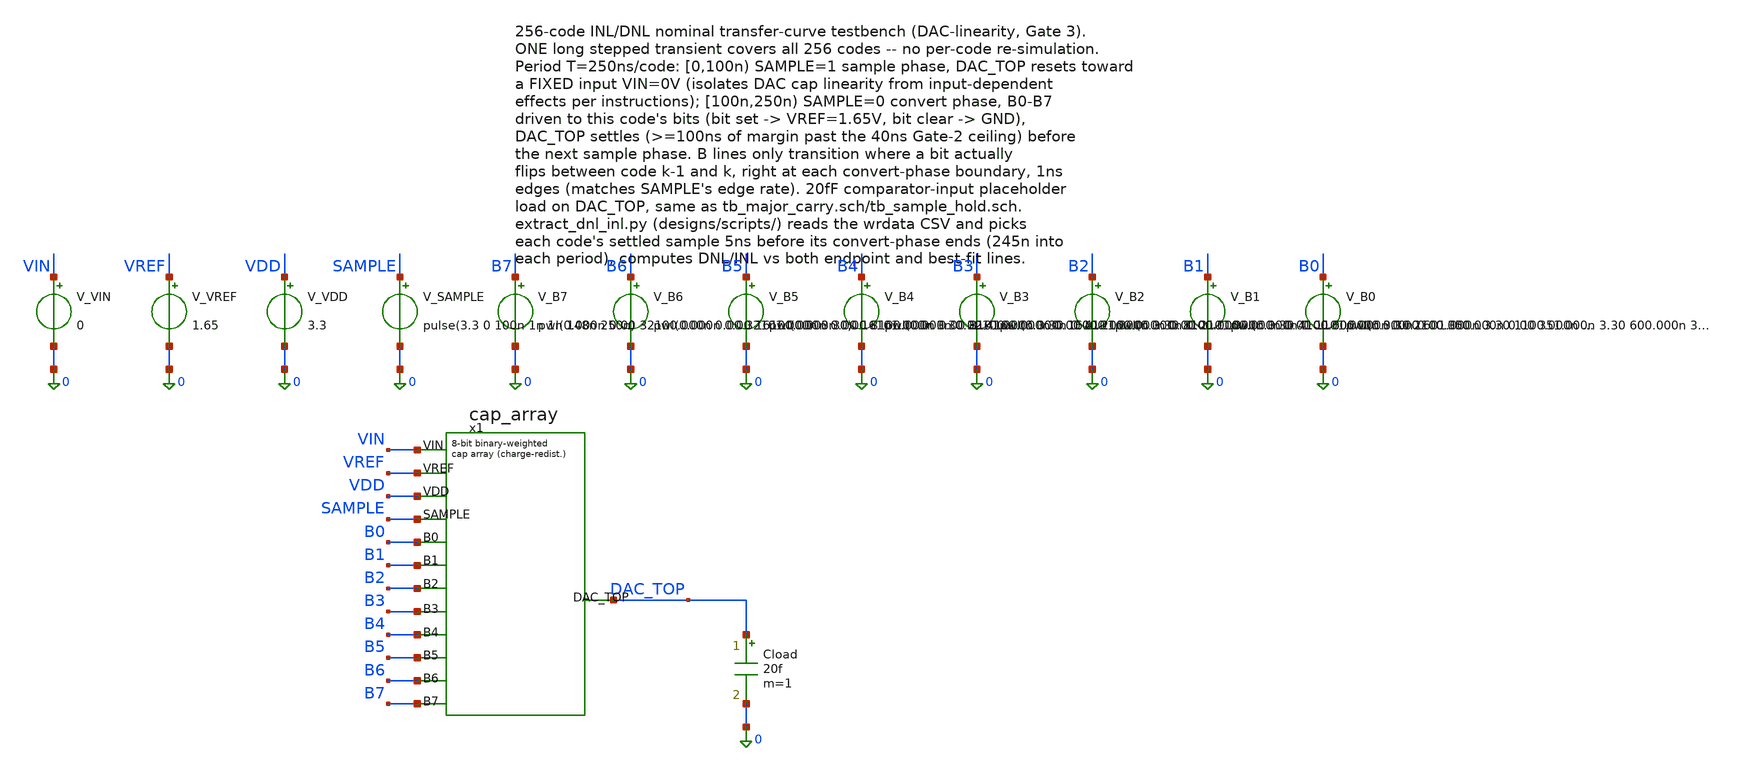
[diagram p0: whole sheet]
** sch_path: dac/sim/tb_inl_dnl.sch
**.subckt tb_inl_dnl
V_VIN VIN 0 0
V_VREF VREF 0 1.65
V_VDD VDD 0 3.3
V_SAMPLE SAMPLE 0 pulse(3.3 0 100n 1n 1n 148n 250n)
V_B7 B7 0 pwl(0.000n 0.00 32100.000n 0.00 32101.000n 3.30)
V_B6 B6 0 pwl(0.000n 0.00 16100.000n 0.00 16101.000n 3.30 32100.000n 3.30 32101.000n 0.00 48100.000n
+ 0.00 48101.000n 3.30)
V_B5 B5 0 pwl(0.000n 0.00 8100.000n 0.00 8101.000n 3.30 16100.000n 3.30 16101.000n 0.00 24100.000n
+ 0.00 24101.000n 3.30 32100.000n 3.30 32101.000n 0.00 40100.000n 0.00 40101.000n 3.30 48100.000n 3.30
+ 48101.000n 0.00 56100.000n 0.00 56101.000n 3.30)
V_B4 B4 0 pwl(0.000n 0.00 4100.000n 0.00 4101.000n 3.30 8100.000n 3.30 8101.000n 0.00 12100.000n
+ 0.00 12101.000n 3.30 16100.000n 3.30 16101.000n 0.00 20100.000n 0.00 20101.000n 3.30 24100.000n 3.30
+ 24101.000n 0.00 28100.000n 0.00 28101.000n 3.30 32100.000n 3.30 32101.000n 0.00 36100.000n 0.00 36101.000n
+ 3.30 40100.000n 3.30 40101.000n 0.00 44100.000n 0.00 44101.000n 3.30 48100.000n 3.30 48101.000n 0.00
+ 52100.000n 0.00 52101.000n 3.30 56100.000n 3.30 56101.000n 0.00 60100.000n 0.00 60101.000n 3.30)
V_B3 B3 0 pwl(0.000n 0.00 2100.000n 0.00 2101.000n 3.30 4100.000n 3.30 4101.000n 0.00 6100.000n 0.00
+ 6101.000n 3.30 8100.000n 3.30 8101.000n 0.00 10100.000n 0.00 10101.000n 3.30 12100.000n 3.30 12101.000n 0.00
+ 14100.000n 0.00 14101.000n 3.30 16100.000n 3.30 16101.000n 0.00 18100.000n 0.00 18101.000n 3.30 20100.000n
+ 3.30 20101.000n 0.00 22100.000n 0.00 22101.000n 3.30 24100.000n 3.30 24101.000n 0.00 26100.000n 0.00
+ 26101.000n 3.30 28100.000n 3.30 28101.000n 0.00 30100.000n 0.00 30101.000n 3.30 32100.000n 3.30 32101.000n
+ 0.00 34100.000n 0.00 34101.000n 3.30 36100.000n 3.30 36101.000n 0.00 38100.000n 0.00 38101.000n 3.30
+ 40100.000n 3.30 40101.000n 0.00 42100.000n 0.00 42101.000n 3.30 44100.000n 3.30 44101.000n 0.00 46100.000n
+ 0.00 46101.000n 3.30 48100.000n 3.30 48101.000n 0.00 50100.000n 0.00 50101.000n 3.30 52100.000n 3.30
+ 52101.000n 0.00 54100.000n 0.00 54101.000n 3.30 56100.000n 3.30 56101.000n 0.00 58100.000n 0.00 58101.000n
+ 3.30 60100.000n 3.30 60101.000n 0.00 62100.000n 0.00 62101.000n 3.30)
V_B2 B2 0 pwl(0.000n 0.00 1100.000n 0.00 1101.000n 3.30 2100.000n 3.30 2101.000n 0.00 3100.000n 0.00
+ 3101.000n 3.30 4100.000n 3.30 4101.000n 0.00 5100.000n 0.00 5101.000n 3.30 6100.000n 3.30 6101.000n 0.00
+ 7100.000n 0.00 7101.000n 3.30 8100.000n 3.30 8101.000n 0.00 9100.000n 0.00 9101.000n 3.30 10100.000n 3.30
+ 10101.000n 0.00 11100.000n 0.00 11101.000n 3.30 12100.000n 3.30 12101.000n 0.00 13100.000n 0.00 13101.000n
+ 3.30 14100.000n 3.30 14101.000n 0.00 15100.000n 0.00 15101.000n 3.30 16100.000n 3.30 16101.000n 0.00
+ 17100.000n 0.00 17101.000n 3.30 18100.000n 3.30 18101.000n 0.00 19100.000n 0.00 19101.000n 3.30 20100.000n
+ 3.30 20101.000n 0.00 21100.000n 0.00 21101.000n 3.30 22100.000n 3.30 22101.000n 0.00 23100.000n 0.00
+ 23101.000n 3.30 24100.000n 3.30 24101.000n 0.00 25100.000n 0.00 25101.000n 3.30 26100.000n 3.30 26101.000n
+ 0.00 27100.000n 0.00 27101.000n 3.30 28100.000n 3.30 28101.000n 0.00 29100.000n 0.00 29101.000n 3.30
+ 30100.000n 3.30 30101.000n 0.00 31100.000n 0.00 31101.000n 3.30 32100.000n 3.30 32101.000n 0.00 33100.000n
+ 0.00 33101.000n 3.30 34100.000n 3.30 34101.000n 0.00 35100.000n 0.00 35101.000n 3.30 36100.000n 3.30
+ 36101.000n 0.00 37100.000n 0.00 37101.000n 3.30 38100.000n 3.30 38101.000n 0.00 39100.000n 0.00 39101.000n
+ 3.30 40100.000n 3.30 40101.000n 0.00 41100.000n 0.00 41101.000n 3.30 42100.000n 3.30 42101.000n 0.00
+ 43100.000n 0.00 43101.000n 3.30 44100.000n 3.30 44101.000n 0.00 45100.000n 0.00 45101.000n 3.30 46100.000n
+ 3.30 46101.000n 0.00 47100.000n 0.00 47101.000n 3.30 48100.000n 3.30 48101.000n 0.00 49100.000n 0.00
+ 49101.000n 3.30 50100.000n 3.30 50101.000n 0.00 51100.000n 0.00 51101.000n 3.30 52100.000n 3.30 52101.000n
+ 0.00 53100.000n 0.00 53101.000n 3.30 54100.000n 3.30 54101.000n 0.00 55100.000n 0.00 55101.000n 3.30
+ 56100.000n 3.30 56101.000n 0.00 57100.000n 0.00 57101.000n 3.30 58100.000n 3.30 58101.000n 0.00 59100.000n
+ 0.00 59101.000n 3.30 60100.000n 3.30 60101.000n 0.00 61100.000n 0.00 61101.000n 3.30 62100.000n 3.30
+ 62101.000n 0.00 63100.000n 0.00 63101.000n 3.30)
V_B1 B1 0 pwl(0.000n 0.00 600.000n 0.00 601.000n 3.30 1100.000n 3.30 1101.000n 0.00 1600.000n 0.00
+ 1601.000n 3.30 2100.000n 3.30 2101.000n 0.00 2600.000n 0.00 2601.000n 3.30 3100.000n 3.30 3101.000n 0.00
+ 3600.000n 0.00 3601.000n 3.30 4100.000n 3.30 4101.000n 0.00 4600.000n 0.00 4601.000n 3.30 5100.000n 3.30
+ 5101.000n 0.00 5600.000n 0.00 5601.000n 3.30 6100.000n 3.30 6101.000n 0.00 6600.000n 0.00 6601.000n 3.30
+ 7100.000n 3.30 7101.000n 0.00 7600.000n 0.00 7601.000n 3.30 8100.000n 3.30 8101.000n 0.00 8600.000n 0.00
+ 8601.000n 3.30 9100.000n 3.30 9101.000n 0.00 9600.000n 0.00 9601.000n 3.30 10100.000n 3.30 10101.000n 0.00
+ 10600.000n 0.00 10601.000n 3.30 11100.000n 3.30 11101.000n 0.00 11600.000n 0.00 11601.000n 3.30 12100.000n
+ 3.30 12101.000n 0.00 12600.000n 0.00 12601.000n 3.30 13100.000n 3.30 13101.000n 0.00 13600.000n 0.00
+ 13601.000n 3.30 14100.000n 3.30 14101.000n 0.00 14600.000n 0.00 14601.000n 3.30 15100.000n 3.30 15101.000n
+ 0.00 15600.000n 0.00 15601.000n 3.30 16100.000n 3.30 16101.000n 0.00 16600.000n 0.00 16601.000n 3.30
+ 17100.000n 3.30 17101.000n 0.00 17600.000n 0.00 17601.000n 3.30 18100.000n 3.30 18101.000n 0.00 18600.000n
+ 0.00 18601.000n 3.30 19100.000n 3.30 19101.000n 0.00 19600.000n 0.00 19601.000n 3.30 20100.000n 3.30
+ 20101.000n 0.00 20600.000n 0.00 20601.000n 3.30 21100.000n 3.30 21101.000n 0.00 21600.000n 0.00 21601.000n
+ 3.30 22100.000n 3.30 22101.000n 0.00 22600.000n 0.00 22601.000n 3.30 23100.000n 3.30 23101.000n 0.00
+ 23600.000n 0.00 23601.000n 3.30 24100.000n 3.30 24101.000n 0.00 24600.000n 0.00 24601.000n 3.30 25100.000n
+ 3.30 25101.000n 0.00 25600.000n 0.00 25601.000n 3.30 26100.000n 3.30 26101.000n 0.00 26600.000n 0.00
+ 26601.000n 3.30 27100.000n 3.30 27101.000n 0.00 27600.000n 0.00 27601.000n 3.30 28100.000n 3.30 28101.000n
+ 0.00 28600.000n 0.00 28601.000n 3.30 29100.000n 3.30 29101.000n 0.00 29600.000n 0.00 29601.000n 3.30
+ 30100.000n 3.30 30101.000n 0.00 30600.000n 0.00 30601.000n 3.30 31100.000n 3.30 31101.000n 0.00 31600.000n
+ 0.00 31601.000n 3.30 32100.000n 3.30 32101.000n 0.00 32600.000n 0.00 32601.000n 3.30 33100.000n 3.30
+ 33101.000n 0.00 33600.000n 0.00 33601.000n 3.30 34100.000n 3.30 34101.000n 0.00 34600.000n 0.00 34601.000n
+ 3.30 35100.000n 3.30 35101.000n 0.00 35600.000n 0.00 35601.000n 3.30 36100.000n 3.30 36101.000n 0.00
+ 36600.000n 0.00 36601.000n 3.30 37100.000n 3.30 37101.000n 0.00 37600.000n 0.00 37601.000n 3.30 38100.000n
+ 3.30 38101.000n 0.00 38600.000n 0.00 38601.000n 3.30 39100.000n 3.30 39101.000n 0.00 39600.000n 0.00
+ 39601.000n 3.30 40100.000n 3.30 40101.000n 0.00 40600.000n 0.00 40601.000n 3.30 41100.000n 3.30 41101.000n
+ 0.00 41600.000n 0.00 41601.000n 3.30 42100.000n 3.30 42101.000n 0.00 42600.000n 0.00 42601.000n 3.30
+ 43100.000n 3.30 43101.000n 0.00 43600.000n 0.00 43601.000n 3.30 44100.000n 3.30 44101.000n 0.00 44600.000n
+ 0.00 44601.000n 3.30 45100.000n 3.30 45101.000n 0.00 45600.000n 0.00 45601.000n 3.30 46100.000n 3.30
+ 46101.000n 0.00 46600.000n 0.00 46601.000n 3.30 47100.000n 3.30 47101.000n 0.00 47600.000n 0.00 47601.000n
+ 3.30 48100.000n 3.30 48101.000n 0.00 48600.000n 0.00 48601.000n 3.30 49100.000n 3.30 49101.000n 0.00
+ 49600.000n 0.00 49601.000n 3.30 50100.000n 3.30 50101.000n 0.00 50600.000n 0.00 50601.000n 3.30 51100.000n
+ 3.30 51101.000n 0.00 51600.000n 0.00 51601.000n 3.30 52100.000n 3.30 52101.000n 0.00 52600.000n 0.00
+ 52601.000n 3.30 53100.000n 3.30 53101.000n 0.00 53600.000n 0.00 53601.000n 3.30 54100.000n 3.30 54101.000n
+ 0.00 54600.000n 0.00 54601.000n 3.30 55100.000n 3.30 55101.000n 0.00 55600.000n 0.00 55601.000n 3.30
+ 56100.000n 3.30 56101.000n 0.00 56600.000n 0.00 56601.000n 3.30 57100.000n 3.30 57101.000n 0.00 57600.000n
+ 0.00 57601.000n 3.30 58100.000n 3.30 58101.000n 0.00 58600.000n 0.00 58601.000n 3.30 59100.000n 3.30
+ 59101.000n 0.00 59600.000n 0.00 59601.000n 3.30 60100.000n 3.30 60101.000n 0.00 60600.000n 0.00 60601.000n
+ 3.30 61100.000n 3.30 61101.000n 0.00 61600.000n 0.00 61601.000n 3.30 62100.000n 3.30 62101.000n 0.00
+ 62600.000n 0.00 62601.000n 3.30 63100.000n 3.30 63101.000n 0.00 63600.000n 0.00 63601.000n 3.30)
V_B0 B0 0 pwl(0.000n 0.00 350.000n 0.00 351.000n 3.30 600.000n 3.30 601.000n 0.00 850.000n 0.00
+ 851.000n 3.30 1100.000n 3.30 1101.000n 0.00 1350.000n 0.00 1351.000n 3.30 1600.000n 3.30 1601.000n 0.00
+ 1850.000n 0.00 1851.000n 3.30 2100.000n 3.30 2101.000n 0.00 2350.000n 0.00 2351.000n 3.30 2600.000n 3.30
+ 2601.000n 0.00 2850.000n 0.00 2851.000n 3.30 3100.000n 3.30 3101.000n 0.00 3350.000n 0.00 3351.000n 3.30
+ 3600.000n 3.30 3601.000n 0.00 3850.000n 0.00 3851.000n 3.30 4100.000n 3.30 4101.000n 0.00 4350.000n 0.00
+ 4351.000n 3.30 4600.000n 3.30 4601.000n 0.00 4850.000n 0.00 4851.000n 3.30 5100.000n 3.30 5101.000n 0.00
+ 5350.000n 0.00 5351.000n 3.30 5600.000n 3.30 5601.000n 0.00 5850.000n 0.00 5851.000n 3.30 6100.000n 3.30
+ 6101.000n 0.00 6350.000n 0.00 6351.000n 3.30 6600.000n 3.30 6601.000n 0.00 6850.000n 0.00 6851.000n 3.30
+ 7100.000n 3.30 7101.000n 0.00 7350.000n 0.00 7351.000n 3.30 7600.000n 3.30 7601.000n 0.00 7850.000n 0.00
+ 7851.000n 3.30 8100.000n 3.30 8101.000n 0.00 8350.000n 0.00 8351.000n 3.30 8600.000n 3.30 8601.000n 0.00
+ 8850.000n 0.00 8851.000n 3.30 9100.000n 3.30 9101.000n 0.00 9350.000n 0.00 9351.000n 3.30 9600.000n 3.30
+ 9601.000n 0.00 9850.000n 0.00 9851.000n 3.30 10100.000n 3.30 10101.000n 0.00 10350.000n 0.00 10351.000n 3.30
+ 10600.000n 3.30 10601.000n 0.00 10850.000n 0.00 10851.000n 3.30 11100.000n 3.30 11101.000n 0.00 11350.000n
+ 0.00 11351.000n 3.30 11600.000n 3.30 11601.000n 0.00 11850.000n 0.00 11851.000n 3.30 12100.000n 3.30
+ 12101.000n 0.00 12350.000n 0.00 12351.000n 3.30 12600.000n 3.30 12601.000n 0.00 12850.000n 0.00 12851.000n
+ 3.30 13100.000n 3.30 13101.000n 0.00 13350.000n 0.00 13351.000n 3.30 13600.000n 3.30 13601.000n 0.00
+ 13850.000n 0.00 13851.000n 3.30 14100.000n 3.30 14101.000n 0.00 14350.000n 0.00 14351.000n 3.30 14600.000n
+ 3.30 14601.000n 0.00 14850.000n 0.00 14851.000n 3.30 15100.000n 3.30 15101.000n 0.00 15350.000n 0.00
+ 15351.000n 3.30 15600.000n 3.30 15601.000n 0.00 15850.000n 0.00 15851.000n 3.30 16100.000n 3.30 16101.000n
+ 0.00 16350.000n 0.00 16351.000n 3.30 16600.000n 3.30 16601.000n 0.00 16850.000n 0.00 16851.000n 3.30
+ 17100.000n 3.30 17101.000n 0.00 17350.000n 0.00 17351.000n 3.30 17600.000n 3.30 17601.000n 0.00 17850.000n
+ 0.00 17851.000n 3.30 18100.000n 3.30 18101.000n 0.00 18350.000n 0.00 18351.000n 3.30 18600.000n 3.30
+ 18601.000n 0.00 18850.000n 0.00 18851.000n 3.30 19100.000n 3.30 19101.000n 0.00 19350.000n 0.00 19351.000n
+ 3.30 19600.000n 3.30 19601.000n 0.00 19850.000n 0.00 19851.000n 3.30 20100.000n 3.30 20101.000n 0.00
+ 20350.000n 0.00 20351.000n 3.30 20600.000n 3.30 20601.000n 0.00 20850.000n 0.00 20851.000n 3.30 21100.000n
+ 3.30 21101.000n 0.00 21350.000n 0.00 21351.000n 3.30 21600.000n 3.30 21601.000n 0.00 21850.000n 0.00
+ 21851.000n 3.30 22100.000n 3.30 22101.000n 0.00 22350.000n 0.00 22351.000n 3.30 22600.000n 3.30 22601.000n
+ 0.00 22850.000n 0.00 22851.000n 3.30 23100.000n 3.30 23101.000n 0.00 23350.000n 0.00 23351.000n 3.30
+ 23600.000n 3.30 23601.000n 0.00 23850.000n 0.00 23851.000n 3.30 24100.000n 3.30 24101.000n 0.00 24350.000n
+ 0.00 24351.000n 3.30 24600.000n 3.30 24601.000n 0.00 24850.000n 0.00 24851.000n 3.30 25100.000n 3.30
+ 25101.000n 0.00 25350.000n 0.00 25351.000n 3.30 25600.000n 3.30 25601.000n 0.00 25850.000n 0.00 25851.000n
+ 3.30 26100.000n 3.30 26101.000n 0.00 26350.000n 0.00 26351.000n 3.30 26600.000n 3.30 26601.000n 0.00
+ 26850.000n 0.00 26851.000n 3.30 27100.000n 3.30 27101.000n 0.00 27350.000n 0.00 27351.000n 3.30 27600.000n
+ 3.30 27601.000n 0.00 27850.000n 0.00 27851.000n 3.30 28100.000n 3.30 28101.000n 0.00 28350.000n 0.00
+ 28351.000n 3.30 28600.000n 3.30 28601.000n 0.00 28850.000n 0.00 28851.000n 3.30 29100.000n 3.30 29101.000n
+ 0.00 29350.000n 0.00 29351.000n 3.30 29600.000n 3.30 29601.000n 0.00 29850.000n 0.00 29851.000n 3.30
+ 30100.000n 3.30 30101.000n 0.00 30350.000n 0.00 30351.000n 3.30 30600.000n 3.30 30601.000n 0.00 30850.000n
+ 0.00 30851.000n 3.30 31100.000n 3.30 31101.000n 0.00 31350.000n 0.00 31351.000n 3.30 31600.000n 3.30
+ 31601.000n 0.00 31850.000n 0.00 31851.000n 3.30 32100.000n 3.30 32101.000n 0.00 32350.000n 0.00 32351.000n
+ 3.30 32600.000n 3.30 32601.000n 0.00 32850.000n 0.00 32851.000n 3.30 33100.000n 3.30 33101.000n 0.00
+ 33350.000n 0.00 33351.000n 3.30 33600.000n 3.30 33601.000n 0.00 33850.000n 0.00 33851.000n 3.30 34100.000n
+ 3.30 34101.000n 0.00 34350.000n 0.00 34351.000n 3.30 34600.000n 3.30 34601.000n 0.00 34850.000n 0.00
+ 34851.000n 3.30 35100.000n 3.30 35101.000n 0.00 35350.000n 0.00 35351.000n 3.30 35600.000n 3.30 35601.000n
+ 0.00 35850.000n 0.00 35851.000n 3.30 36100.000n 3.30 36101.000n 0.00 36350.000n 0.00 36351.000n 3.30
+ 36600.000n 3.30 36601.000n 0.00 36850.000n 0.00 36851.000n 3.30 37100.000n 3.30 37101.000n 0.00 37350.000n
+ 0.00 37351.000n 3.30 37600.000n 3.30 37601.000n 0.00 37850.000n 0.00 37851.000n 3.30 38100.000n 3.30
+ 38101.000n 0.00 38350.000n 0.00 38351.000n 3.30 38600.000n 3.30 38601.000n 0.00 38850.000n 0.00 38851.000n
+ 3.30 39100.000n 3.30 39101.000n 0.00 39350.000n 0.00 39351.000n 3.30 39600.000n 3.30 39601.000n 0.00
+ 39850.000n 0.00 39851.000n 3.30 40100.000n 3.30 40101.000n 0.00 40350.000n 0.00 40351.000n 3.30 40600.000n
+ 3.30 40601.000n 0.00 40850.000n 0.00 40851.000n 3.30 41100.000n 3.30 41101.000n 0.00 41350.000n 0.00
+ 41351.000n 3.30 41600.000n 3.30 41601.000n 0.00 41850.000n 0.00 41851.000n 3.30 42100.000n 3.30 42101.000n
+ 0.00 42350.000n 0.00 42351.000n 3.30 42600.000n 3.30 42601.000n 0.00 42850.000n 0.00 42851.000n 3.30
+ 43100.000n 3.30 43101.000n 0.00 43350.000n 0.00 43351.000n 3.30 43600.000n 3.30 43601.000n 0.00 43850.000n
+ 0.00 43851.000n 3.30 44100.000n 3.30 44101.000n 0.00 44350.000n 0.00 44351.000n 3.30 44600.000n 3.30
+ 44601.000n 0.00 44850.000n 0.00 44851.000n 3.30 45100.000n 3.30 45101.000n 0.00 45350.000n 0.00 45351.000n
+ 3.30 45600.000n 3.30 45601.000n 0.00 45850.000n 0.00 45851.000n 3.30 46100.000n 3.30 46101.000n 0.00
+ 46350.000n 0.00 46351.000n 3.30 46600.000n 3.30 46601.000n 0.00 46850.000n 0.00 46851.000n 3.30 47100.000n
+ 3.30 47101.000n 0.00 47350.000n 0.00 47351.000n 3.30 47600.000n 3.30 47601.000n 0.00 47850.000n 0.00
+ 47851.000n 3.30 48100.000n 3.30 48101.000n 0.00 48350.000n 0.00 48351.000n 3.30 48600.000n 3.30 48601.000n
+ 0.00 48850.000n 0.00 48851.000n 3.30 49100.000n 3.30 49101.000n 0.00 49350.000n 0.00 49351.000n 3.30
+ 49600.000n 3.30 49601.000n 0.00 49850.000n 0.00 49851.000n 3.30 50100.000n 3.30 50101.000n 0.00 50350.000n
+ 0.00 50351.000n 3.30 50600.000n 3.30 50601.000n 0.00 50850.000n 0.00 50851.000n 3.30 51100.000n 3.30
+ 51101.000n 0.00 51350.000n 0.00 51351.000n 3.30 51600.000n 3.30 51601.000n 0.00 51850.000n 0.00 51851.000n
+ 3.30 52100.000n 3.30 52101.000n 0.00 52350.000n 0.00 52351.000n 3.30 52600.000n 3.30 52601.000n 0.00
+ 52850.000n 0.00 52851.000n 3.30 53100.000n 3.30 53101.000n 0.00 53350.000n 0.00 53351.000n 3.30 53600.000n
+ 3.30 53601.000n 0.00 53850.000n 0.00 53851.000n 3.30 54100.000n 3.30 54101.000n 0.00 54350.000n 0.00
+ 54351.000n 3.30 54600.000n 3.30 54601.000n 0.00 54850.000n 0.00 54851.000n 3.30 55100.000n 3.30 55101.000n
+ 0.00 55350.000n 0.00 55351.000n 3.30 55600.000n 3.30 55601.000n 0.00 55850.000n 0.00 55851.000n 3.30
+ 56100.000n 3.30 56101.000n 0.00 56350.000n 0.00 56351.000n 3.30 56600.000n 3.30 56601.000n 0.00 56850.000n
+ 0.00 56851.000n 3.30 57100.000n 3.30 57101.000n 0.00 57350.000n 0.00 57351.000n 3.30 57600.000n 3.30
+ 57601.000n 0.00 57850.000n 0.00 57851.000n 3.30 58100.000n 3.30 58101.000n 0.00 58350.000n 0.00 58351.000n
+ 3.30 58600.000n 3.30 58601.000n 0.00 58850.000n 0.00 58851.000n 3.30 59100.000n 3.30 59101.000n 0.00
+ 59350.000n 0.00 59351.000n 3.30 59600.000n 3.30 59601.000n 0.00 59850.000n 0.00 59851.000n 3.30 60100.000n
+ 3.30 60101.000n 0.00 60350.000n 0.00 60351.000n 3.30 60600.000n 3.30 60601.000n 0.00 60850.000n 0.00
+ 60851.000n 3.30 61100.000n 3.30 61101.000n 0.00 61350.000n 0.00 61351.000n 3.30 61600.000n 3.30 61601.000n
+ 0.00 61850.000n 0.00 61851.000n 3.30 62100.000n 3.30 62101.000n 0.00 62350.000n 0.00 62351.000n 3.30
+ 62600.000n 3.30 62601.000n 0.00 62850.000n 0.00 62851.000n 3.30 63100.000n 3.30 63101.000n 0.00 63350.000n
+ 0.00 63351.000n 3.30 63600.000n 3.30 63601.000n 0.00 63850.000n 0.00 63851.000n 3.30)
Cload DAC_TOP 0 20f m=1
x1 VIN VREF VDD SAMPLE B0 B1 B2 B3 B4 B5 B6 B7 DAC_TOP cap_array
**** begin user architecture code


.param nfet_wid=0.42u nfet_len=0.28u
.param mim_corner_1p0fF=1 mim_corner_1p5fF=1 mim_corner_2p0fF=1
.param mc_c_cox_1p0fF=0 mc_c_cox_1p5fF=0 mc_c_cox_2p0fF=0
.param var_vth=0 var_k=0
.lib /foss/pdks/gf180mcuD/libs.tech/ngspice/sm141064.ngspice typical
.lib /foss/pdks/gf180mcuD/libs.tech/ngspice/sm141064.ngspice cap_mim
.include /foss/pdks/gf180mcuD/libs.tech/ngspice/design.ngspice
.control
* uic + default-zero initial conditions (no explicit .ic needed: VIN=0
* already matches the desired DAC_TOP=0 cold start). 'save all' at this
* timestep/duration blows ngspice's default output-memory limit (same
* issue documented in the 2026-07-17 figures-export WORKLOG entry) --
* save only the node this analysis needs.
save v(dac_top)
tran 1n 64u uic
wrdata dac/sim/tb_inl_dnl_tran.csv v(DAC_TOP)
.endc


**** end user architecture code
**.ends
.end
